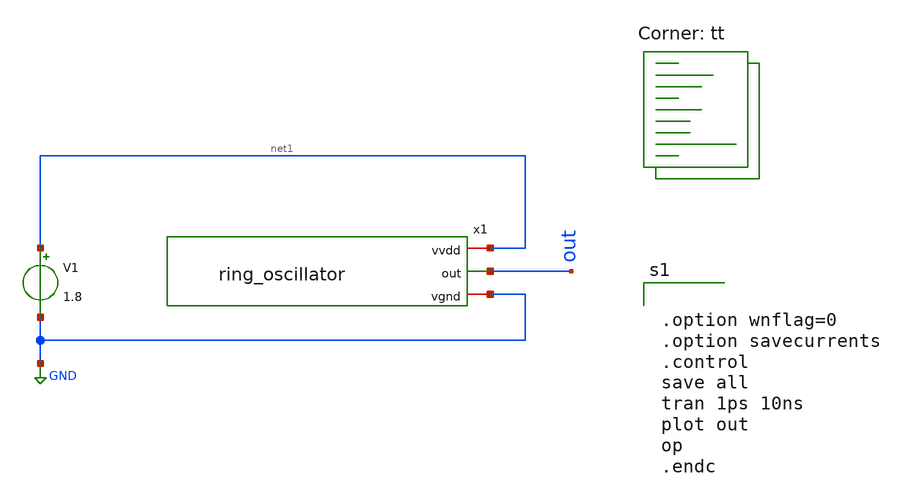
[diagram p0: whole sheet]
** sch_path: oscillator/ring_oscillator_tb.sch
**.subckt ring_oscillator_tb
x1 net1 out GND ring_oscillator
V1 net1 GND 1.8
**** begin user architecture code
.lib $::SKYWATER_MODELS/sky130.lib.spice tt


.option wnflag=0
.option savecurrents
.control
save all
tran 1ps 10ns
plot out
op
.endc


**** end user architecture code
**.ends

* expanding   symbol:  ring_oscillator.sym # of pins=3
** sym_path: oscillator/ring_oscillator.sym
** sch_path: oscillator/ring_oscillator.sch
.subckt ring_oscillator vvdd out vgnd
*.iopin vvdd
*.iopin vgnd
*.opin out
x1 vvdd out net1 vgnd iinverter
x2 vvdd net1 net2 vgnd iinverter
x3 vvdd net2 out vgnd iinverter
.ends


* expanding   symbol:  /home/deboradmk/project1/iinverter.sym # of pins=4
** sym_path: iinverter/iinverter.sym
** sch_path: iinverter/iinverter.sch
.subckt iinverter vvdd in out vgnd
*.ipin vvdd
*.ipin in
*.ipin vgnd
*.opin out
XM3 out in vgnd vgnd sky130_fd_pr__nfet_01v8 L=0.15 W=1 nf=1 ad='int((nf+1)/2) * W/nf * 0.29' as='int((nf+2)/2) * W/nf * 0.29'
+ pd='2*int((nf+1)/2) * (W/nf + 0.29)' ps='2*int((nf+2)/2) * (W/nf + 0.29)' nrd='0.29 / W' nrs='0.29 / W'
+ sa=0 sb=0 sd=0 mult=1 m=1
XM2 out in vvdd vvdd sky130_fd_pr__pfet_01v8 L=0.15 W=1 nf=1 ad='int((nf+1)/2) * W/nf * 0.29' as='int((nf+2)/2) * W/nf * 0.29'
+ pd='2*int((nf+1)/2) * (W/nf + 0.29)' ps='2*int((nf+2)/2) * (W/nf + 0.29)' nrd='0.29 / W' nrs='0.29 / W'
+ sa=0 sb=0 sd=0 mult=1 m=1
.ends

.GLOBAL GND
.end
